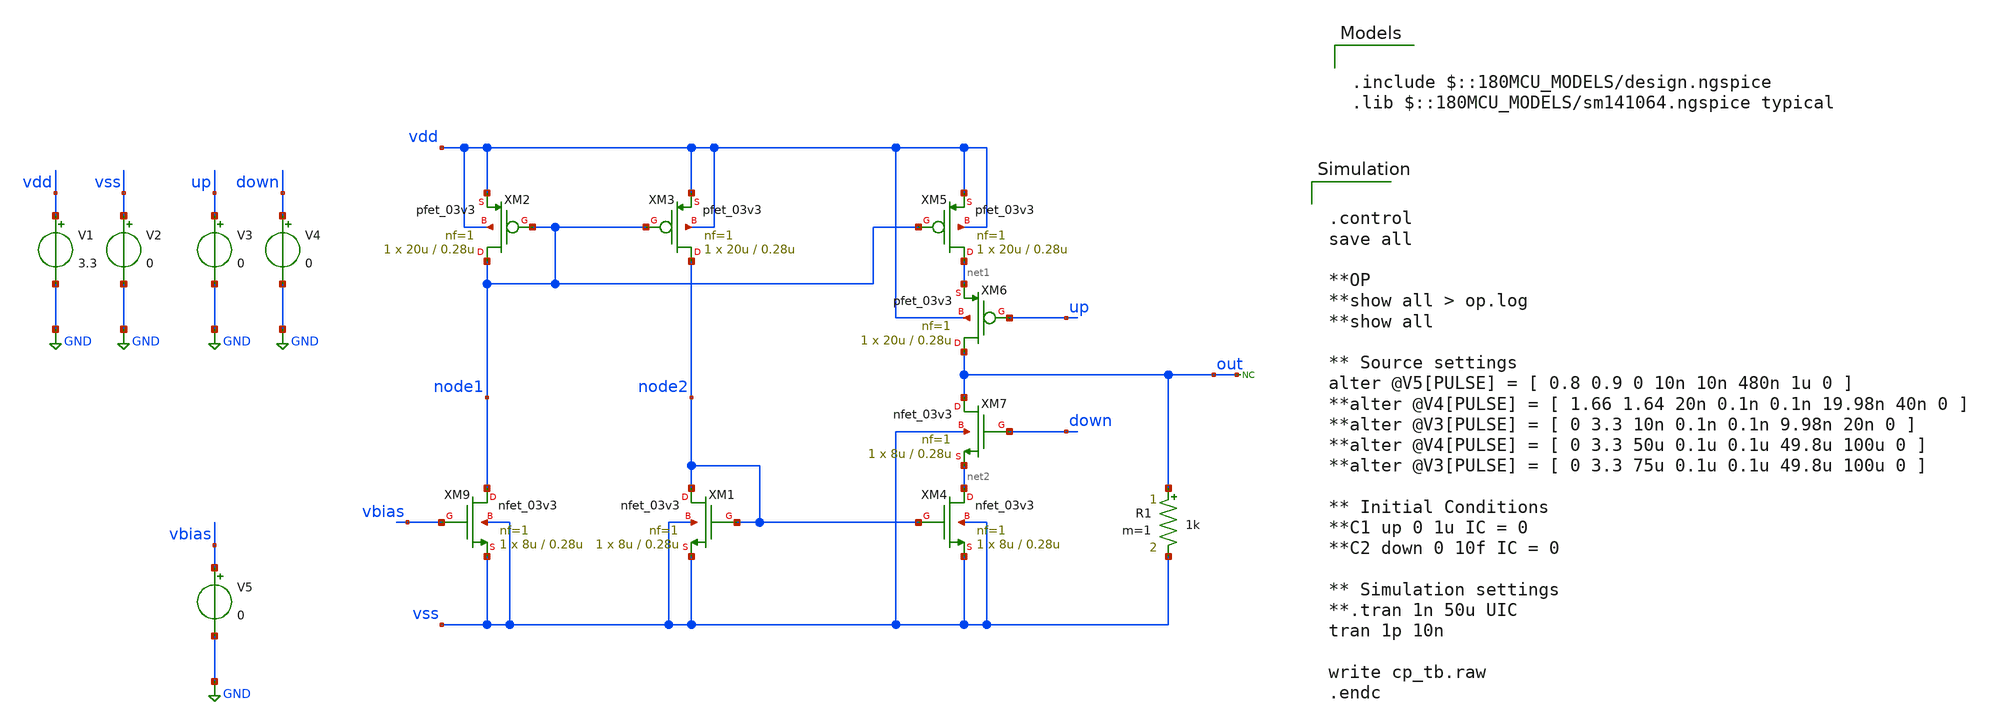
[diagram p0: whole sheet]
** sch_path: designs/libs/qw_core_analog_pkedit/CPforVCO.sch
**.subckt CPforVCO
XM1 node2 node2 vss vss nfet_03v3 L=0.28u W=8u nf=1 ad='int((nf+1)/2) * W/nf * 0.18u' as='int((nf+2)/2) * W/nf * 0.18u'
+ pd='2*int((nf+1)/2) * (W/nf + 0.18u)' ps='2*int((nf+2)/2) * (W/nf + 0.18u)' nrd='0.18u / W' nrs='0.18u / W'
+ sa=0 sb=0 sd=0 m=1
XM2 node1 node1 vdd vdd pfet_03v3 L=0.28u W=20u nf=1 ad='int((nf+1)/2) * W/nf * 0.18u' as='int((nf+2)/2) * W/nf * 0.18u'
+ pd='2*int((nf+1)/2) * (W/nf + 0.18u)' ps='2*int((nf+2)/2) * (W/nf + 0.18u)' nrd='0.18u / W' nrs='0.18u / W'
+ sa=0 sb=0 sd=0 m=1
XM3 node2 node1 vdd vdd pfet_03v3 L=0.28u W=20u nf=1 ad='int((nf+1)/2) * W/nf * 0.18u' as='int((nf+2)/2) * W/nf * 0.18u'
+ pd='2*int((nf+1)/2) * (W/nf + 0.18u)' ps='2*int((nf+2)/2) * (W/nf + 0.18u)' nrd='0.18u / W' nrs='0.18u / W'
+ sa=0 sb=0 sd=0 m=1
XM4 net2 node2 vss vss nfet_03v3 L=0.28u W=8u nf=1 ad='int((nf+1)/2) * W/nf * 0.18u' as='int((nf+2)/2) * W/nf * 0.18u'
+ pd='2*int((nf+1)/2) * (W/nf + 0.18u)' ps='2*int((nf+2)/2) * (W/nf + 0.18u)' nrd='0.18u / W' nrs='0.18u / W'
+ sa=0 sb=0 sd=0 m=1
XM5 net1 node1 vdd vdd pfet_03v3 L=0.28u W=20u nf=1 ad='int((nf+1)/2) * W/nf * 0.18u' as='int((nf+2)/2) * W/nf * 0.18u'
+ pd='2*int((nf+1)/2) * (W/nf + 0.18u)' ps='2*int((nf+2)/2) * (W/nf + 0.18u)' nrd='0.18u / W' nrs='0.18u / W'
+ sa=0 sb=0 sd=0 m=1
XM6 out up net1 vdd pfet_03v3 L=0.28u W=20u nf=1 ad='int((nf+1)/2) * W/nf * 0.18u' as='int((nf+2)/2) * W/nf * 0.18u'
+ pd='2*int((nf+1)/2) * (W/nf + 0.18u)' ps='2*int((nf+2)/2) * (W/nf + 0.18u)' nrd='0.18u / W' nrs='0.18u / W'
+ sa=0 sb=0 sd=0 m=1
XM7 out down net2 vss nfet_03v3 L=0.28u W=8u nf=1 ad='int((nf+1)/2) * W/nf * 0.18u' as='int((nf+2)/2) * W/nf * 0.18u'
+ pd='2*int((nf+1)/2) * (W/nf + 0.18u)' ps='2*int((nf+2)/2) * (W/nf + 0.18u)' nrd='0.18u / W' nrs='0.18u / W'
+ sa=0 sb=0 sd=0 m=1
V1 vdd GND 3.3
V2 vss GND 0
* noconn out
V3 up GND 0
V4 down GND 0
R1 out vss 1k m=1
XM9 node1 vbias vss vss nfet_03v3 L=0.28u W=8u nf=1 ad='int((nf+1)/2) * W/nf * 0.18u' as='int((nf+2)/2) * W/nf * 0.18u'
+ pd='2*int((nf+1)/2) * (W/nf + 0.18u)' ps='2*int((nf+2)/2) * (W/nf + 0.18u)' nrd='0.18u / W' nrs='0.18u / W'
+ sa=0 sb=0 sd=0 m=1
V5 vbias GND 0
**** begin user architecture code

.include $::180MCU_MODELS/design.ngspice
.lib $::180MCU_MODELS/sm141064.ngspice typical



.control
save all

**OP
**show all > op.log
**show all

** Source settings
alter @V5[PULSE] = [ 0.8 0.9 0 10n 10n 480n 1u 0 ]
**alter @V4[PULSE] = [ 1.66 1.64 20n 0.1n 0.1n 19.98n 40n 0 ]
**alter @V3[PULSE] = [ 0 3.3 10n 0.1n 0.1n 9.98n 20n 0 ]
**alter @V4[PULSE] = [ 0 3.3 50u 0.1u 0.1u 49.8u 100u 0 ]
**alter @V3[PULSE] = [ 0 3.3 75u 0.1u 0.1u 49.8u 100u 0 ]

** Initial Conditions
**C1 up 0 1u IC = 0
**C2 down 0 10f IC = 0

** Simulation settings
**.tran 1n 50u UIC
tran 1p 10n

write cp_tb.raw
.endc


**** end user architecture code
**.ends
.GLOBAL GND
.end
